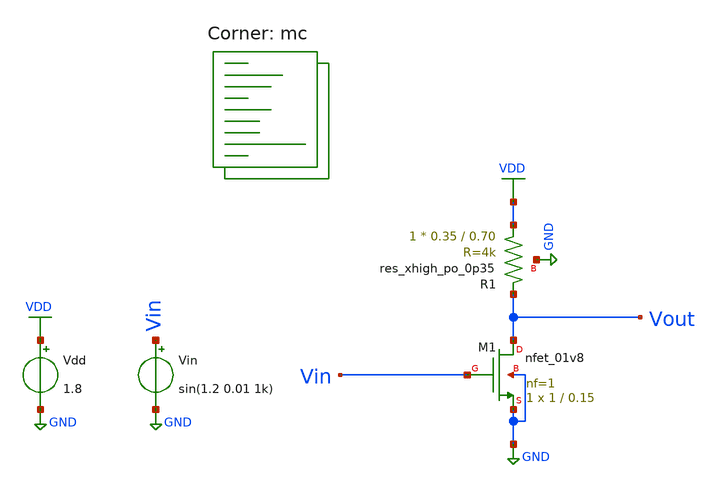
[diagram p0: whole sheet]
** sch_path: projects/montecarlo/xschem_ngspice/inverter/common_source_mc.sch
**.subckt common_source_mc
XM1 Vout Vin GND GND sky130_fd_pr__nfet_01v8 L=0.15 W=1 nf=1 ad='int((nf+1)/2) * W/nf * 0.29' as='int((nf+2)/2) * W/nf * 0.29'
+ pd='2*int((nf+1)/2) * (W/nf + 0.29)' ps='2*int((nf+2)/2) * (W/nf + 0.29)' nrd='0.29 / W' nrs='0.29 / W'
+ sa=0 sb=0 sd=0 mult=1 m=1
Vdd VDD GND 1.8
Vin Vin GND sin(1.2 0.01 1k)
XR1 VDD Vout GND sky130_fd_pr__res_xhigh_po_0p35 L=0.70 mult=1 m=1
**** begin user architecture code



.option wnflag=1
.option savecurrents
.save @m.xm1.msky130_fd_pr__nfet_01v8[gm] @m.xm1.msky130_fd_pr__nfet_01v8[vth] @m.xm2.msky130_fd_pr__pfet_01v8[gm] @m.xm2.msky130_fd_pr__pfet_01v8[vth]

.control

  let runs=100
  let run=1

  dowhile run <= runs
    save all
    * dc vin 0 1.8 0.01
    tran 1u 3m
    write common_source_mc.raw
    set appendwrite
    reset
    let run = run + 1
  end

.endc



.lib $::SKYWATER_MODELS/sky130.lib.spice mc
**** end user architecture code
**.ends
.GLOBAL VDD
.GLOBAL GND
.end
